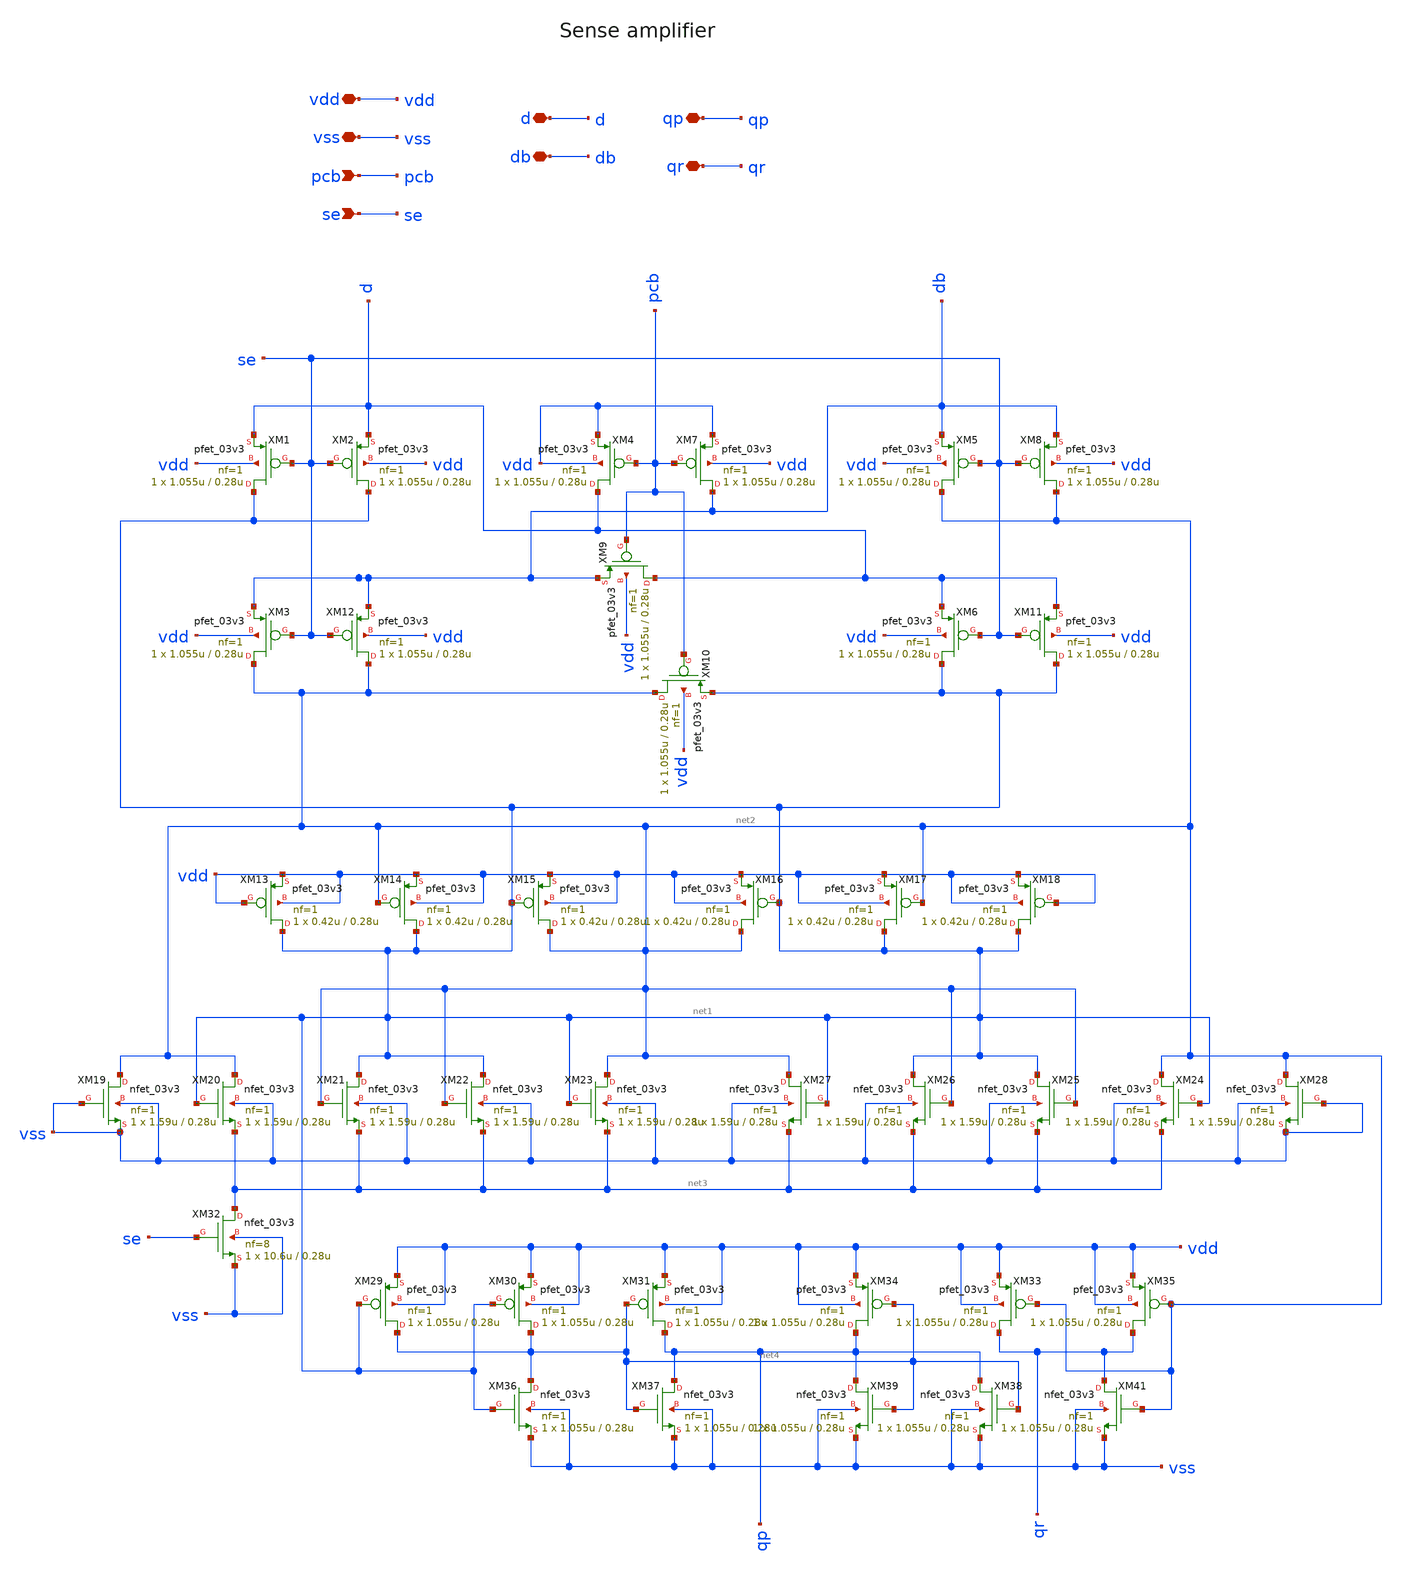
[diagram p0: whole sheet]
** sch_path: cells/gf180mcu_ocd_ip_sram__sram512x8m8wm1/xschem/sa_3v512x8m81.sch
**.subckt sa_3v512x8m81 pcb se vdd vss d db qp qr
*.ipin pcb
*.ipin se
*.iopin vdd
*.iopin vss
*.iopin d
*.iopin db
*.iopin qp
*.iopin qr
XM1 net1 se d vdd pfet_03v3 L=0.28u W=1.055u nf=1 ad='int((nf+1)/2) * W/nf * 0.18u' as='int((nf+2)/2) * W/nf * 0.18u'
+ pd='2*int((nf+1)/2) * (W/nf + 0.18u)' ps='2*int((nf+2)/2) * (W/nf + 0.18u)' nrd='0.18u / W' nrs='0.18u / W'
+ sa=0 sb=0 sd=0 m=1
XM2 net1 se d vdd pfet_03v3 L=0.28u W=1.055u nf=1 ad='int((nf+1)/2) * W/nf * 0.18u' as='int((nf+2)/2) * W/nf * 0.18u'
+ pd='2*int((nf+1)/2) * (W/nf + 0.18u)' ps='2*int((nf+2)/2) * (W/nf + 0.18u)' nrd='0.18u / W' nrs='0.18u / W'
+ sa=0 sb=0 sd=0 m=1
XM9 d pcb db vdd pfet_03v3 L=0.28u W=1.055u nf=1 ad='int((nf+1)/2) * W/nf * 0.18u' as='int((nf+2)/2) * W/nf * 0.18u'
+ pd='2*int((nf+1)/2) * (W/nf + 0.18u)' ps='2*int((nf+2)/2) * (W/nf + 0.18u)' nrd='0.18u / W' nrs='0.18u / W'
+ sa=0 sb=0 sd=0 m=1
XM10 net2 pcb net1 vdd pfet_03v3 L=0.28u W=1.055u nf=1 ad='int((nf+1)/2) * W/nf * 0.18u' as='int((nf+2)/2) * W/nf * 0.18u'
+ pd='2*int((nf+1)/2) * (W/nf + 0.18u)' ps='2*int((nf+2)/2) * (W/nf + 0.18u)' nrd='0.18u / W' nrs='0.18u / W'
+ sa=0 sb=0 sd=0 m=1
XM13 net1 vdd vdd vdd pfet_03v3 L=0.28u W=0.42u nf=1 ad='int((nf+1)/2) * W/nf * 0.18u' as='int((nf+2)/2) * W/nf * 0.18u'
+ pd='2*int((nf+1)/2) * (W/nf + 0.18u)' ps='2*int((nf+2)/2) * (W/nf + 0.18u)' nrd='0.18u / W' nrs='0.18u / W'
+ sa=0 sb=0 sd=0 m=1
XM14 net1 net2 vdd vdd pfet_03v3 L=0.28u W=0.42u nf=1 ad='int((nf+1)/2) * W/nf * 0.18u' as='int((nf+2)/2) * W/nf * 0.18u'
+ pd='2*int((nf+1)/2) * (W/nf + 0.18u)' ps='2*int((nf+2)/2) * (W/nf + 0.18u)' nrd='0.18u / W' nrs='0.18u / W'
+ sa=0 sb=0 sd=0 m=1
XM15 net2 net1 vdd vdd pfet_03v3 L=0.28u W=0.42u nf=1 ad='int((nf+1)/2) * W/nf * 0.18u' as='int((nf+2)/2) * W/nf * 0.18u'
+ pd='2*int((nf+1)/2) * (W/nf + 0.18u)' ps='2*int((nf+2)/2) * (W/nf + 0.18u)' nrd='0.18u / W' nrs='0.18u / W'
+ sa=0 sb=0 sd=0 m=1
XM16 net2 net1 vdd vdd pfet_03v3 L=0.28u W=0.42u nf=1 ad='int((nf+1)/2) * W/nf * 0.18u' as='int((nf+2)/2) * W/nf * 0.18u'
+ pd='2*int((nf+1)/2) * (W/nf + 0.18u)' ps='2*int((nf+2)/2) * (W/nf + 0.18u)' nrd='0.18u / W' nrs='0.18u / W'
+ sa=0 sb=0 sd=0 m=1
XM17 net1 net2 vdd vdd pfet_03v3 L=0.28u W=0.42u nf=1 ad='int((nf+1)/2) * W/nf * 0.18u' as='int((nf+2)/2) * W/nf * 0.18u'
+ pd='2*int((nf+1)/2) * (W/nf + 0.18u)' ps='2*int((nf+2)/2) * (W/nf + 0.18u)' nrd='0.18u / W' nrs='0.18u / W'
+ sa=0 sb=0 sd=0 m=1
XM18 net1 vdd vdd vdd pfet_03v3 L=0.28u W=0.42u nf=1 ad='int((nf+1)/2) * W/nf * 0.18u' as='int((nf+2)/2) * W/nf * 0.18u'
+ pd='2*int((nf+1)/2) * (W/nf + 0.18u)' ps='2*int((nf+2)/2) * (W/nf + 0.18u)' nrd='0.18u / W' nrs='0.18u / W'
+ sa=0 sb=0 sd=0 m=1
XM19 net2 vss vss vss nfet_03v3 L=0.28u W=1.59u nf=1 ad='int((nf+1)/2) * W/nf * 0.18u' as='int((nf+2)/2) * W/nf * 0.18u'
+ pd='2*int((nf+1)/2) * (W/nf + 0.18u)' ps='2*int((nf+2)/2) * (W/nf + 0.18u)' nrd='0.18u / W' nrs='0.18u / W'
+ sa=0 sb=0 sd=0 m=1
XM28 net2 vss vss vss nfet_03v3 L=0.28u W=1.59u nf=1 ad='int((nf+1)/2) * W/nf * 0.18u' as='int((nf+2)/2) * W/nf * 0.18u'
+ pd='2*int((nf+1)/2) * (W/nf + 0.18u)' ps='2*int((nf+2)/2) * (W/nf + 0.18u)' nrd='0.18u / W' nrs='0.18u / W'
+ sa=0 sb=0 sd=0 m=1
XM32 net3 se vss vss nfet_03v3 L=0.28u W=10.6u nf=8 ad='int((nf+1)/2) * W/nf * 0.18u' as='int((nf+2)/2) * W/nf * 0.18u'
+ pd='2*int((nf+1)/2) * (W/nf + 0.18u)' ps='2*int((nf+2)/2) * (W/nf + 0.18u)' nrd='0.18u / W' nrs='0.18u / W'
+ sa=0 sb=0 sd=0 m=1
XM29 net4 net1 vdd vdd pfet_03v3 L=0.28u W=1.055u nf=1 ad='int((nf+1)/2) * W/nf * 0.18u' as='int((nf+2)/2) * W/nf * 0.18u'
+ pd='2*int((nf+1)/2) * (W/nf + 0.18u)' ps='2*int((nf+2)/2) * (W/nf + 0.18u)' nrd='0.18u / W' nrs='0.18u / W'
+ sa=0 sb=0 sd=0 m=1
XM35 qr net2 vdd vdd pfet_03v3 L=0.28u W=1.055u nf=1 ad='int((nf+1)/2) * W/nf * 0.18u' as='int((nf+2)/2) * W/nf * 0.18u'
+ pd='2*int((nf+1)/2) * (W/nf + 0.18u)' ps='2*int((nf+2)/2) * (W/nf + 0.18u)' nrd='0.18u / W' nrs='0.18u / W'
+ sa=0 sb=0 sd=0 m=1
XM36 net4 net1 vss vss nfet_03v3 L=0.28u W=1.055u nf=1 ad='int((nf+1)/2) * W/nf * 0.18u' as='int((nf+2)/2) * W/nf * 0.18u'
+ pd='2*int((nf+1)/2) * (W/nf + 0.18u)' ps='2*int((nf+2)/2) * (W/nf + 0.18u)' nrd='0.18u / W' nrs='0.18u / W'
+ sa=0 sb=0 sd=0 m=1
XM41 qr net2 vss vss nfet_03v3 L=0.28u W=1.055u nf=1 ad='int((nf+1)/2) * W/nf * 0.18u' as='int((nf+2)/2) * W/nf * 0.18u'
+ pd='2*int((nf+1)/2) * (W/nf + 0.18u)' ps='2*int((nf+2)/2) * (W/nf + 0.18u)' nrd='0.18u / W' nrs='0.18u / W'
+ sa=0 sb=0 sd=0 m=1
XM3 net2 se db vdd pfet_03v3 L=0.28u W=1.055u nf=1 ad='int((nf+1)/2) * W/nf * 0.18u' as='int((nf+2)/2) * W/nf * 0.18u'
+ pd='2*int((nf+1)/2) * (W/nf + 0.18u)' ps='2*int((nf+2)/2) * (W/nf + 0.18u)' nrd='0.18u / W' nrs='0.18u / W'
+ sa=0 sb=0 sd=0 m=1
XM4 d pcb vdd vdd pfet_03v3 L=0.28u W=1.055u nf=1 ad='int((nf+1)/2) * W/nf * 0.18u' as='int((nf+2)/2) * W/nf * 0.18u'
+ pd='2*int((nf+1)/2) * (W/nf + 0.18u)' ps='2*int((nf+2)/2) * (W/nf + 0.18u)' nrd='0.18u / W' nrs='0.18u / W'
+ sa=0 sb=0 sd=0 m=1
XM5 net2 se db vdd pfet_03v3 L=0.28u W=1.055u nf=1 ad='int((nf+1)/2) * W/nf * 0.18u' as='int((nf+2)/2) * W/nf * 0.18u'
+ pd='2*int((nf+1)/2) * (W/nf + 0.18u)' ps='2*int((nf+2)/2) * (W/nf + 0.18u)' nrd='0.18u / W' nrs='0.18u / W'
+ sa=0 sb=0 sd=0 m=1
XM6 net1 se d vdd pfet_03v3 L=0.28u W=1.055u nf=1 ad='int((nf+1)/2) * W/nf * 0.18u' as='int((nf+2)/2) * W/nf * 0.18u'
+ pd='2*int((nf+1)/2) * (W/nf + 0.18u)' ps='2*int((nf+2)/2) * (W/nf + 0.18u)' nrd='0.18u / W' nrs='0.18u / W'
+ sa=0 sb=0 sd=0 m=1
XM7 db pcb vdd vdd pfet_03v3 L=0.28u W=1.055u nf=1 ad='int((nf+1)/2) * W/nf * 0.18u' as='int((nf+2)/2) * W/nf * 0.18u'
+ pd='2*int((nf+1)/2) * (W/nf + 0.18u)' ps='2*int((nf+2)/2) * (W/nf + 0.18u)' nrd='0.18u / W' nrs='0.18u / W'
+ sa=0 sb=0 sd=0 m=1
XM8 net2 se db vdd pfet_03v3 L=0.28u W=1.055u nf=1 ad='int((nf+1)/2) * W/nf * 0.18u' as='int((nf+2)/2) * W/nf * 0.18u'
+ pd='2*int((nf+1)/2) * (W/nf + 0.18u)' ps='2*int((nf+2)/2) * (W/nf + 0.18u)' nrd='0.18u / W' nrs='0.18u / W'
+ sa=0 sb=0 sd=0 m=1
XM11 net1 se d vdd pfet_03v3 L=0.28u W=1.055u nf=1 ad='int((nf+1)/2) * W/nf * 0.18u' as='int((nf+2)/2) * W/nf * 0.18u'
+ pd='2*int((nf+1)/2) * (W/nf + 0.18u)' ps='2*int((nf+2)/2) * (W/nf + 0.18u)' nrd='0.18u / W' nrs='0.18u / W'
+ sa=0 sb=0 sd=0 m=1
XM12 net2 se db vdd pfet_03v3 L=0.28u W=1.055u nf=1 ad='int((nf+1)/2) * W/nf * 0.18u' as='int((nf+2)/2) * W/nf * 0.18u'
+ pd='2*int((nf+1)/2) * (W/nf + 0.18u)' ps='2*int((nf+2)/2) * (W/nf + 0.18u)' nrd='0.18u / W' nrs='0.18u / W'
+ sa=0 sb=0 sd=0 m=1
XM20 net2 net1 net3 vss nfet_03v3 L=0.28u W=1.59u nf=1 ad='int((nf+1)/2) * W/nf * 0.18u' as='int((nf+2)/2) * W/nf * 0.18u'
+ pd='2*int((nf+1)/2) * (W/nf + 0.18u)' ps='2*int((nf+2)/2) * (W/nf + 0.18u)' nrd='0.18u / W' nrs='0.18u / W'
+ sa=0 sb=0 sd=0 m=1
XM21 net1 net2 net3 vss nfet_03v3 L=0.28u W=1.59u nf=1 ad='int((nf+1)/2) * W/nf * 0.18u' as='int((nf+2)/2) * W/nf * 0.18u'
+ pd='2*int((nf+1)/2) * (W/nf + 0.18u)' ps='2*int((nf+2)/2) * (W/nf + 0.18u)' nrd='0.18u / W' nrs='0.18u / W'
+ sa=0 sb=0 sd=0 m=1
XM22 net1 net2 net3 vss nfet_03v3 L=0.28u W=1.59u nf=1 ad='int((nf+1)/2) * W/nf * 0.18u' as='int((nf+2)/2) * W/nf * 0.18u'
+ pd='2*int((nf+1)/2) * (W/nf + 0.18u)' ps='2*int((nf+2)/2) * (W/nf + 0.18u)' nrd='0.18u / W' nrs='0.18u / W'
+ sa=0 sb=0 sd=0 m=1
XM23 net2 net1 net3 vss nfet_03v3 L=0.28u W=1.59u nf=1 ad='int((nf+1)/2) * W/nf * 0.18u' as='int((nf+2)/2) * W/nf * 0.18u'
+ pd='2*int((nf+1)/2) * (W/nf + 0.18u)' ps='2*int((nf+2)/2) * (W/nf + 0.18u)' nrd='0.18u / W' nrs='0.18u / W'
+ sa=0 sb=0 sd=0 m=1
XM24 net2 net1 net3 vss nfet_03v3 L=0.28u W=1.59u nf=1 ad='int((nf+1)/2) * W/nf * 0.18u' as='int((nf+2)/2) * W/nf * 0.18u'
+ pd='2*int((nf+1)/2) * (W/nf + 0.18u)' ps='2*int((nf+2)/2) * (W/nf + 0.18u)' nrd='0.18u / W' nrs='0.18u / W'
+ sa=0 sb=0 sd=0 m=1
XM25 net1 net2 net3 vss nfet_03v3 L=0.28u W=1.59u nf=1 ad='int((nf+1)/2) * W/nf * 0.18u' as='int((nf+2)/2) * W/nf * 0.18u'
+ pd='2*int((nf+1)/2) * (W/nf + 0.18u)' ps='2*int((nf+2)/2) * (W/nf + 0.18u)' nrd='0.18u / W' nrs='0.18u / W'
+ sa=0 sb=0 sd=0 m=1
XM26 net1 net2 net3 vss nfet_03v3 L=0.28u W=1.59u nf=1 ad='int((nf+1)/2) * W/nf * 0.18u' as='int((nf+2)/2) * W/nf * 0.18u'
+ pd='2*int((nf+1)/2) * (W/nf + 0.18u)' ps='2*int((nf+2)/2) * (W/nf + 0.18u)' nrd='0.18u / W' nrs='0.18u / W'
+ sa=0 sb=0 sd=0 m=1
XM27 net2 net1 net3 vss nfet_03v3 L=0.28u W=1.59u nf=1 ad='int((nf+1)/2) * W/nf * 0.18u' as='int((nf+2)/2) * W/nf * 0.18u'
+ pd='2*int((nf+1)/2) * (W/nf + 0.18u)' ps='2*int((nf+2)/2) * (W/nf + 0.18u)' nrd='0.18u / W' nrs='0.18u / W'
+ sa=0 sb=0 sd=0 m=1
XM30 net4 net1 vdd vdd pfet_03v3 L=0.28u W=1.055u nf=1 ad='int((nf+1)/2) * W/nf * 0.18u' as='int((nf+2)/2) * W/nf * 0.18u'
+ pd='2*int((nf+1)/2) * (W/nf + 0.18u)' ps='2*int((nf+2)/2) * (W/nf + 0.18u)' nrd='0.18u / W' nrs='0.18u / W'
+ sa=0 sb=0 sd=0 m=1
XM31 qp net4 vdd vdd pfet_03v3 L=0.28u W=1.055u nf=1 ad='int((nf+1)/2) * W/nf * 0.18u' as='int((nf+2)/2) * W/nf * 0.18u'
+ pd='2*int((nf+1)/2) * (W/nf + 0.18u)' ps='2*int((nf+2)/2) * (W/nf + 0.18u)' nrd='0.18u / W' nrs='0.18u / W'
+ sa=0 sb=0 sd=0 m=1
XM33 qr net2 vdd vdd pfet_03v3 L=0.28u W=1.055u nf=1 ad='int((nf+1)/2) * W/nf * 0.18u' as='int((nf+2)/2) * W/nf * 0.18u'
+ pd='2*int((nf+1)/2) * (W/nf + 0.18u)' ps='2*int((nf+2)/2) * (W/nf + 0.18u)' nrd='0.18u / W' nrs='0.18u / W'
+ sa=0 sb=0 sd=0 m=1
XM34 qp net4 vdd vdd pfet_03v3 L=0.28u W=1.055u nf=1 ad='int((nf+1)/2) * W/nf * 0.18u' as='int((nf+2)/2) * W/nf * 0.18u'
+ pd='2*int((nf+1)/2) * (W/nf + 0.18u)' ps='2*int((nf+2)/2) * (W/nf + 0.18u)' nrd='0.18u / W' nrs='0.18u / W'
+ sa=0 sb=0 sd=0 m=1
XM37 qp net4 vss vss nfet_03v3 L=0.28u W=1.055u nf=1 ad='int((nf+1)/2) * W/nf * 0.18u' as='int((nf+2)/2) * W/nf * 0.18u'
+ pd='2*int((nf+1)/2) * (W/nf + 0.18u)' ps='2*int((nf+2)/2) * (W/nf + 0.18u)' nrd='0.18u / W' nrs='0.18u / W'
+ sa=0 sb=0 sd=0 m=1
XM38 qp net4 vss vss nfet_03v3 L=0.28u W=1.055u nf=1 ad='int((nf+1)/2) * W/nf * 0.18u' as='int((nf+2)/2) * W/nf * 0.18u'
+ pd='2*int((nf+1)/2) * (W/nf + 0.18u)' ps='2*int((nf+2)/2) * (W/nf + 0.18u)' nrd='0.18u / W' nrs='0.18u / W'
+ sa=0 sb=0 sd=0 m=1
XM39 qp net4 vss vss nfet_03v3 L=0.28u W=1.055u nf=1 ad='int((nf+1)/2) * W/nf * 0.18u' as='int((nf+2)/2) * W/nf * 0.18u'
+ pd='2*int((nf+1)/2) * (W/nf + 0.18u)' ps='2*int((nf+2)/2) * (W/nf + 0.18u)' nrd='0.18u / W' nrs='0.18u / W'
+ sa=0 sb=0 sd=0 m=1
**.ends
.end
